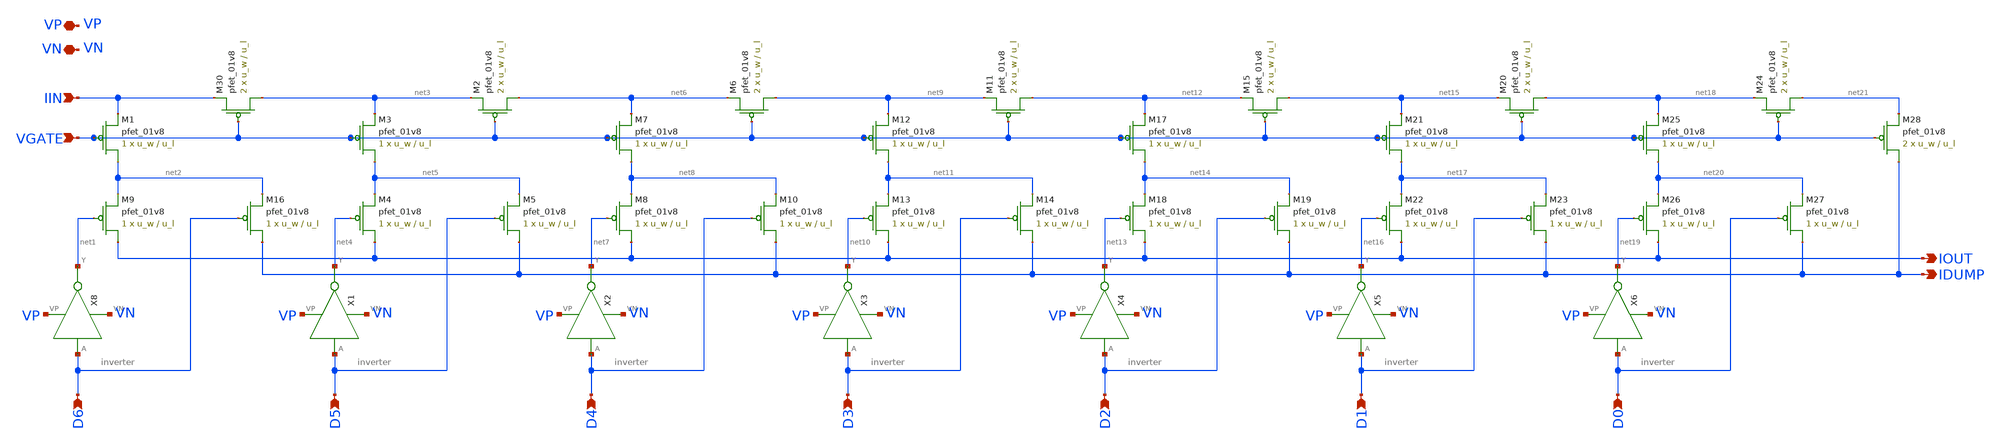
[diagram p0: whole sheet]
** sch_path: lib/analog/schematic/m2m_ladder.sch
**.subckt m2m_ladder VN VP IIN VGATE D6 D5 D4 D3 D2 D1 D0 IOUT IDUMP
*.iopin VN
*.iopin VP
*.ipin IIN
*.ipin VGATE
*.ipin D6
*.ipin D5
*.ipin D4
*.ipin D3
*.ipin D2
*.ipin D1
*.ipin D0
*.opin IOUT
*.opin IDUMP
X8 D6 net1 VP VN inverter
XM30 net3 VGATE IIN VDD sky130_fd_pr__pfet_01v8 L=u_l W=u_w nf=1 ad='int((nf+1)/2) * W/nf * 0.29' as='int((nf+2)/2) * W/nf * 0.29'
+ pd='2*int((nf+1)/2) * (W/nf + 0.29)' ps='2*int((nf+2)/2) * (W/nf + 0.29)' nrd='0.29 / W' nrs='0.29 / W'
+ sa=0 sb=0 sd=0 mult=2 m=2
XM1 net2 VGATE IIN VDD sky130_fd_pr__pfet_01v8 L=u_l W=u_w nf=1 ad='int((nf+1)/2) * W/nf * 0.29' as='int((nf+2)/2) * W/nf * 0.29'
+ pd='2*int((nf+1)/2) * (W/nf + 0.29)' ps='2*int((nf+2)/2) * (W/nf + 0.29)' nrd='0.29 / W' nrs='0.29 / W'
+ sa=0 sb=0 sd=0 mult=1 m=1
XM9 IOUT net1 net2 VDD sky130_fd_pr__pfet_01v8 L=u_l W=u_w nf=1 ad='int((nf+1)/2) * W/nf * 0.29' as='int((nf+2)/2) * W/nf * 0.29'
+ pd='2*int((nf+1)/2) * (W/nf + 0.29)' ps='2*int((nf+2)/2) * (W/nf + 0.29)' nrd='0.29 / W' nrs='0.29 / W'
+ sa=0 sb=0 sd=0 mult=1 m=1
XM16 IDUMP D6 net2 VDD sky130_fd_pr__pfet_01v8 L=u_l W=u_w nf=1 ad='int((nf+1)/2) * W/nf * 0.29' as='int((nf+2)/2) * W/nf * 0.29'
+ pd='2*int((nf+1)/2) * (W/nf + 0.29)' ps='2*int((nf+2)/2) * (W/nf + 0.29)' nrd='0.29 / W' nrs='0.29 / W'
+ sa=0 sb=0 sd=0 mult=1 m=1
XM2 net6 VGATE net3 VDD sky130_fd_pr__pfet_01v8 L=u_l W=u_w nf=1 ad='int((nf+1)/2) * W/nf * 0.29' as='int((nf+2)/2) * W/nf * 0.29'
+ pd='2*int((nf+1)/2) * (W/nf + 0.29)' ps='2*int((nf+2)/2) * (W/nf + 0.29)' nrd='0.29 / W' nrs='0.29 / W'
+ sa=0 sb=0 sd=0 mult=2 m=2
XM3 net5 VGATE net3 VDD sky130_fd_pr__pfet_01v8 L=u_l W=u_w nf=1 ad='int((nf+1)/2) * W/nf * 0.29' as='int((nf+2)/2) * W/nf * 0.29'
+ pd='2*int((nf+1)/2) * (W/nf + 0.29)' ps='2*int((nf+2)/2) * (W/nf + 0.29)' nrd='0.29 / W' nrs='0.29 / W'
+ sa=0 sb=0 sd=0 mult=1 m=1
XM4 IOUT net4 net5 VDD sky130_fd_pr__pfet_01v8 L=u_l W=u_w nf=1 ad='int((nf+1)/2) * W/nf * 0.29' as='int((nf+2)/2) * W/nf * 0.29'
+ pd='2*int((nf+1)/2) * (W/nf + 0.29)' ps='2*int((nf+2)/2) * (W/nf + 0.29)' nrd='0.29 / W' nrs='0.29 / W'
+ sa=0 sb=0 sd=0 mult=1 m=1
XM5 IDUMP D5 net5 VDD sky130_fd_pr__pfet_01v8 L=u_l W=u_w nf=1 ad='int((nf+1)/2) * W/nf * 0.29' as='int((nf+2)/2) * W/nf * 0.29'
+ pd='2*int((nf+1)/2) * (W/nf + 0.29)' ps='2*int((nf+2)/2) * (W/nf + 0.29)' nrd='0.29 / W' nrs='0.29 / W'
+ sa=0 sb=0 sd=0 mult=1 m=1
XM6 net9 VGATE net6 VDD sky130_fd_pr__pfet_01v8 L=u_l W=u_w nf=1 ad='int((nf+1)/2) * W/nf * 0.29' as='int((nf+2)/2) * W/nf * 0.29'
+ pd='2*int((nf+1)/2) * (W/nf + 0.29)' ps='2*int((nf+2)/2) * (W/nf + 0.29)' nrd='0.29 / W' nrs='0.29 / W'
+ sa=0 sb=0 sd=0 mult=2 m=2
XM7 net8 VGATE net6 VDD sky130_fd_pr__pfet_01v8 L=u_l W=u_w nf=1 ad='int((nf+1)/2) * W/nf * 0.29' as='int((nf+2)/2) * W/nf * 0.29'
+ pd='2*int((nf+1)/2) * (W/nf + 0.29)' ps='2*int((nf+2)/2) * (W/nf + 0.29)' nrd='0.29 / W' nrs='0.29 / W'
+ sa=0 sb=0 sd=0 mult=1 m=1
XM8 IOUT net7 net8 VDD sky130_fd_pr__pfet_01v8 L=u_l W=u_w nf=1 ad='int((nf+1)/2) * W/nf * 0.29' as='int((nf+2)/2) * W/nf * 0.29'
+ pd='2*int((nf+1)/2) * (W/nf + 0.29)' ps='2*int((nf+2)/2) * (W/nf + 0.29)' nrd='0.29 / W' nrs='0.29 / W'
+ sa=0 sb=0 sd=0 mult=1 m=1
XM10 IDUMP D4 net8 VDD sky130_fd_pr__pfet_01v8 L=u_l W=u_w nf=1 ad='int((nf+1)/2) * W/nf * 0.29' as='int((nf+2)/2) * W/nf * 0.29'
+ pd='2*int((nf+1)/2) * (W/nf + 0.29)' ps='2*int((nf+2)/2) * (W/nf + 0.29)' nrd='0.29 / W' nrs='0.29 / W'
+ sa=0 sb=0 sd=0 mult=1 m=1
XM11 net12 VGATE net9 VDD sky130_fd_pr__pfet_01v8 L=u_l W=u_w nf=1 ad='int((nf+1)/2) * W/nf * 0.29' as='int((nf+2)/2) * W/nf * 0.29'
+ pd='2*int((nf+1)/2) * (W/nf + 0.29)' ps='2*int((nf+2)/2) * (W/nf + 0.29)' nrd='0.29 / W' nrs='0.29 / W'
+ sa=0 sb=0 sd=0 mult=2 m=2
XM12 net11 VGATE net9 VDD sky130_fd_pr__pfet_01v8 L=u_l W=u_w nf=1 ad='int((nf+1)/2) * W/nf * 0.29' as='int((nf+2)/2) * W/nf * 0.29'
+ pd='2*int((nf+1)/2) * (W/nf + 0.29)' ps='2*int((nf+2)/2) * (W/nf + 0.29)' nrd='0.29 / W' nrs='0.29 / W'
+ sa=0 sb=0 sd=0 mult=1 m=1
XM13 IOUT net10 net11 VDD sky130_fd_pr__pfet_01v8 L=u_l W=u_w nf=1 ad='int((nf+1)/2) * W/nf * 0.29' as='int((nf+2)/2) * W/nf * 0.29'
+ pd='2*int((nf+1)/2) * (W/nf + 0.29)' ps='2*int((nf+2)/2) * (W/nf + 0.29)' nrd='0.29 / W' nrs='0.29 / W'
+ sa=0 sb=0 sd=0 mult=1 m=1
XM14 IDUMP D3 net11 VDD sky130_fd_pr__pfet_01v8 L=u_l W=u_w nf=1 ad='int((nf+1)/2) * W/nf * 0.29' as='int((nf+2)/2) * W/nf * 0.29'
+ pd='2*int((nf+1)/2) * (W/nf + 0.29)' ps='2*int((nf+2)/2) * (W/nf + 0.29)' nrd='0.29 / W' nrs='0.29 / W'
+ sa=0 sb=0 sd=0 mult=1 m=1
XM15 net15 VGATE net12 VDD sky130_fd_pr__pfet_01v8 L=u_l W=u_w nf=1 ad='int((nf+1)/2) * W/nf * 0.29'
+ as='int((nf+2)/2) * W/nf * 0.29' pd='2*int((nf+1)/2) * (W/nf + 0.29)' ps='2*int((nf+2)/2) * (W/nf + 0.29)'
+ nrd='0.29 / W' nrs='0.29 / W' sa=0 sb=0 sd=0 mult=2 m=2
XM17 net14 VGATE net12 VDD sky130_fd_pr__pfet_01v8 L=u_l W=u_w nf=1 ad='int((nf+1)/2) * W/nf * 0.29'
+ as='int((nf+2)/2) * W/nf * 0.29' pd='2*int((nf+1)/2) * (W/nf + 0.29)' ps='2*int((nf+2)/2) * (W/nf + 0.29)'
+ nrd='0.29 / W' nrs='0.29 / W' sa=0 sb=0 sd=0 mult=1 m=1
XM18 IOUT net13 net14 VDD sky130_fd_pr__pfet_01v8 L=u_l W=u_w nf=1 ad='int((nf+1)/2) * W/nf * 0.29' as='int((nf+2)/2) * W/nf * 0.29'
+ pd='2*int((nf+1)/2) * (W/nf + 0.29)' ps='2*int((nf+2)/2) * (W/nf + 0.29)' nrd='0.29 / W' nrs='0.29 / W'
+ sa=0 sb=0 sd=0 mult=1 m=1
XM19 IDUMP D2 net14 VDD sky130_fd_pr__pfet_01v8 L=u_l W=u_w nf=1 ad='int((nf+1)/2) * W/nf * 0.29' as='int((nf+2)/2) * W/nf * 0.29'
+ pd='2*int((nf+1)/2) * (W/nf + 0.29)' ps='2*int((nf+2)/2) * (W/nf + 0.29)' nrd='0.29 / W' nrs='0.29 / W'
+ sa=0 sb=0 sd=0 mult=1 m=1
XM20 net18 VGATE net15 VDD sky130_fd_pr__pfet_01v8 L=u_l W=u_w nf=1 ad='int((nf+1)/2) * W/nf * 0.29'
+ as='int((nf+2)/2) * W/nf * 0.29' pd='2*int((nf+1)/2) * (W/nf + 0.29)' ps='2*int((nf+2)/2) * (W/nf + 0.29)'
+ nrd='0.29 / W' nrs='0.29 / W' sa=0 sb=0 sd=0 mult=2 m=2
XM21 net17 VGATE net15 VDD sky130_fd_pr__pfet_01v8 L=u_l W=u_w nf=1 ad='int((nf+1)/2) * W/nf * 0.29'
+ as='int((nf+2)/2) * W/nf * 0.29' pd='2*int((nf+1)/2) * (W/nf + 0.29)' ps='2*int((nf+2)/2) * (W/nf + 0.29)'
+ nrd='0.29 / W' nrs='0.29 / W' sa=0 sb=0 sd=0 mult=1 m=1
XM22 IOUT net16 net17 VDD sky130_fd_pr__pfet_01v8 L=u_l W=u_w nf=1 ad='int((nf+1)/2) * W/nf * 0.29' as='int((nf+2)/2) * W/nf * 0.29'
+ pd='2*int((nf+1)/2) * (W/nf + 0.29)' ps='2*int((nf+2)/2) * (W/nf + 0.29)' nrd='0.29 / W' nrs='0.29 / W'
+ sa=0 sb=0 sd=0 mult=1 m=1
XM23 IDUMP D1 net17 VDD sky130_fd_pr__pfet_01v8 L=u_l W=u_w nf=1 ad='int((nf+1)/2) * W/nf * 0.29' as='int((nf+2)/2) * W/nf * 0.29'
+ pd='2*int((nf+1)/2) * (W/nf + 0.29)' ps='2*int((nf+2)/2) * (W/nf + 0.29)' nrd='0.29 / W' nrs='0.29 / W'
+ sa=0 sb=0 sd=0 mult=1 m=1
XM24 net21 VGATE net18 VDD sky130_fd_pr__pfet_01v8 L=u_l W=u_w nf=1 ad='int((nf+1)/2) * W/nf * 0.29'
+ as='int((nf+2)/2) * W/nf * 0.29' pd='2*int((nf+1)/2) * (W/nf + 0.29)' ps='2*int((nf+2)/2) * (W/nf + 0.29)'
+ nrd='0.29 / W' nrs='0.29 / W' sa=0 sb=0 sd=0 mult=2 m=2
XM25 net20 VGATE net18 VDD sky130_fd_pr__pfet_01v8 L=u_l W=u_w nf=1 ad='int((nf+1)/2) * W/nf * 0.29'
+ as='int((nf+2)/2) * W/nf * 0.29' pd='2*int((nf+1)/2) * (W/nf + 0.29)' ps='2*int((nf+2)/2) * (W/nf + 0.29)'
+ nrd='0.29 / W' nrs='0.29 / W' sa=0 sb=0 sd=0 mult=1 m=1
XM26 IOUT net19 net20 VDD sky130_fd_pr__pfet_01v8 L=u_l W=u_w nf=1 ad='int((nf+1)/2) * W/nf * 0.29' as='int((nf+2)/2) * W/nf * 0.29'
+ pd='2*int((nf+1)/2) * (W/nf + 0.29)' ps='2*int((nf+2)/2) * (W/nf + 0.29)' nrd='0.29 / W' nrs='0.29 / W'
+ sa=0 sb=0 sd=0 mult=1 m=1
XM27 IDUMP D0 net20 VDD sky130_fd_pr__pfet_01v8 L=u_l W=u_w nf=1 ad='int((nf+1)/2) * W/nf * 0.29' as='int((nf+2)/2) * W/nf * 0.29'
+ pd='2*int((nf+1)/2) * (W/nf + 0.29)' ps='2*int((nf+2)/2) * (W/nf + 0.29)' nrd='0.29 / W' nrs='0.29 / W'
+ sa=0 sb=0 sd=0 mult=1 m=1
X1 D5 net4 VP VN inverter
X2 D4 net7 VP VN inverter
X3 D3 net10 VP VN inverter
X4 D2 net13 VP VN inverter
X5 D1 net16 VP VN inverter
X6 D0 net19 VP VN inverter
XM28 IDUMP VGATE net21 VDD sky130_fd_pr__pfet_01v8 L=u_l W=u_w nf=1 ad='int((nf+1)/2) * W/nf * 0.29'
+ as='int((nf+2)/2) * W/nf * 0.29' pd='2*int((nf+1)/2) * (W/nf + 0.29)' ps='2*int((nf+2)/2) * (W/nf + 0.29)'
+ nrd='0.29 / W' nrs='0.29 / W' sa=0 sb=0 sd=0 mult=2 m=2
**** begin user architecture code


.param u_w=@u_w u_l=@u_l


**** end user architecture code
**.ends
.end
